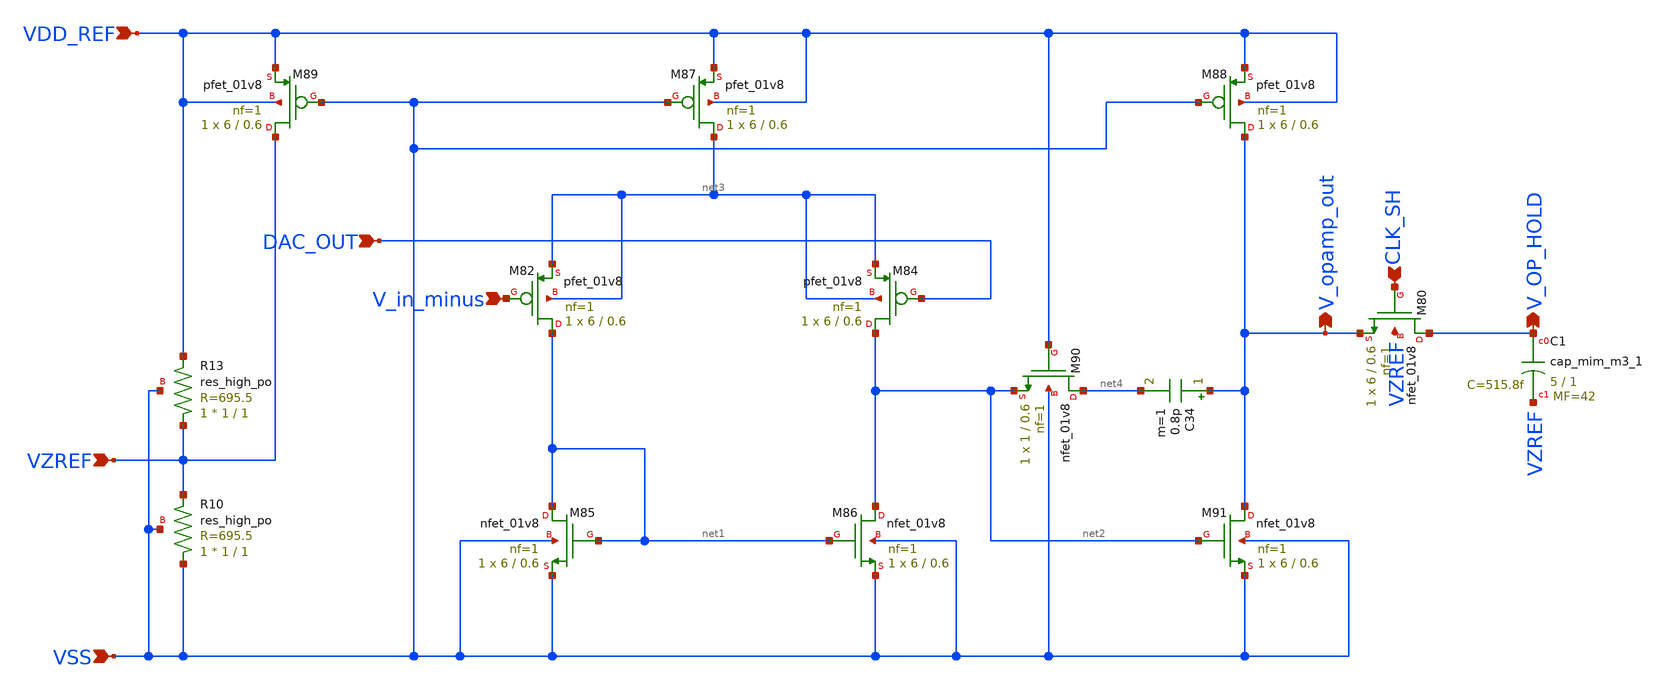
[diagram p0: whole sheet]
** sch_path: 3bit_sar_adc/tb_opamp_hold.sch
**.subckt tb_opamp_hold V_opamp_out DAC_OUT CLK_SH V_OP_HOLD VDD_REF VZREF VSS V_in_minus
*.opin V_opamp_out
*.ipin DAC_OUT
*.ipin CLK_SH
*.opin V_OP_HOLD
*.ipin VDD_REF
*.ipin VZREF
*.ipin VSS
*.ipin V_in_minus
XM82 net1 V_in_minus net3 net3 sky130_fd_pr__pfet_01v8 L=0.6 W=6 nf=1 ad='W * 0.29' as='W * 0.29' pd='2 * (W + 0.29)'
+ ps='2 * (W + 0.29)' nrd='0.29 / W' nrs='0.29 / W' sa=0 sb=0 sd=0 mult=1 m=1
XM84 net2 DAC_OUT net3 net3 sky130_fd_pr__pfet_01v8 L=0.6 W=6 nf=1 ad='W * 0.29' as='W * 0.29' pd='2 * (W + 0.29)'
+ ps='2 * (W + 0.29)' nrd='0.29 / W' nrs='0.29 / W' sa=0 sb=0 sd=0 mult=1 m=1
XM85 net1 net1 VSS VSS sky130_fd_pr__nfet_01v8 L=0.6 W=6 nf=1 ad='W * 0.29' as='W * 0.29' pd='2 * (W + 0.29)'
+ ps='2 * (W + 0.29)' nrd='0.29 / W' nrs='0.29 / W' sa=0 sb=0 sd=0 mult=1 m=1
XM86 net2 net1 VSS VSS sky130_fd_pr__nfet_01v8 L=0.6 W=6 nf=1 ad='W * 0.29' as='W * 0.29' pd='2 * (W + 0.29)'
+ ps='2 * (W + 0.29)' nrd='0.29 / W' nrs='0.29 / W' sa=0 sb=0 sd=0 mult=1 m=1
XM87 net3 VSS VDD_REF VDD_REF sky130_fd_pr__pfet_01v8 L=0.6 W=6 nf=1 ad='W * 0.29' as='W * 0.29' pd='2 * (W + 0.29)'
+ ps='2 * (W + 0.29)' nrd='0.29 / W' nrs='0.29 / W' sa=0 sb=0 sd=0 mult=1 m=1
XM88 V_opamp_out VSS VDD_REF VDD_REF sky130_fd_pr__pfet_01v8 L=0.6 W=6 nf=1 ad='W * 0.29' as='W * 0.29'
+ pd='2 * (W + 0.29)' ps='2 * (W + 0.29)' nrd='0.29 / W' nrs='0.29 / W' sa=0 sb=0 sd=0 mult=1 m=1
XM89 VZREF VSS VDD_REF VDD_REF sky130_fd_pr__pfet_01v8 L=0.6 W=6 nf=1 ad='W * 0.29' as='W * 0.29' pd='2 * (W + 0.29)'
+ ps='2 * (W + 0.29)' nrd='0.29 / W' nrs='0.29 / W' sa=0 sb=0 sd=0 mult=1 m=1
XM90 net4 VDD_REF net2 VSS sky130_fd_pr__nfet_01v8 L=0.6 W=1 nf=1 ad='W * 0.29' as='W * 0.29' pd='2 * (W + 0.29)'
+ ps='2 * (W + 0.29)' nrd='0.29 / W' nrs='0.29 / W' sa=0 sb=0 sd=0 mult=1 m=1
XM91 V_opamp_out net2 VSS VSS sky130_fd_pr__nfet_01v8 L=0.6 W=6 nf=1 ad='W * 0.29' as='W * 0.29' pd='2 * (W + 0.29)'
+ ps='2 * (W + 0.29)' nrd='0.29 / W' nrs='0.29 / W' sa=0 sb=0 sd=0 mult=1 m=1
XR10 VSS VZREF VSS sky130_fd_pr__res_high_po W=1 L=1 mult=1 m=1
XR13 VZREF VDD_REF VSS sky130_fd_pr__res_high_po W=1 L=1 mult=1 m=1
C34 V_opamp_out net4 0.8p m=1
XM80 V_OP_HOLD CLK_SH V_opamp_out VZREF sky130_fd_pr__nfet_01v8 L=0.6 W=6 nf=1 ad='W * 0.29' as='W * 0.29'
+ pd='2 * (W + 0.29)' ps='2 * (W + 0.29)' nrd='0.29 / W' nrs='0.29 / W' sa=0 sb=0 sd=0 mult=1 m=1
XC1 V_OP_HOLD VZREF sky130_fd_pr__cap_mim_m3_1 W=5 L=1 MF=42 m=42
**** begin user architecture code

** opencircuitdesign pdks install
.lib $::SKYWATER_MODELS/sky130.lib.spice tt
.include $::SKYWATER_STDCELLS/sky130_fd_sc_hd.spice
.include /foss/pdks/sky130A/libs.tech/xschem/sky130_stdcells/




.option savecurrents
.options gmin=1e-12 reltol=1e-3 abstol=1e-12
.options method=gear
VANALOG ANALOG 0 SIN(0.9 0.9 200k 50n)
VVDD_REF VDD_REF 0 DC 3.3
VVSS VSS 0 DC -1.8
VVZREF VZREF 0 DC 0
VCLK_SH CLK_SH 0 PULSE(0 3.3 0 0.1n 0.1n 500n 1000n)

.control
save all
  tran 50n 250u
  remzerovec
  write tb_opamp_hold.raw
.endc


**** end user architecture code
**.ends
.end
